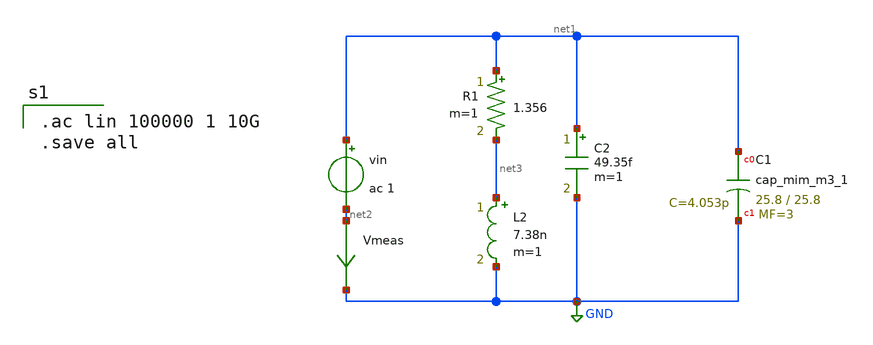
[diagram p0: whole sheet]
** sch_path: XSCHEM/ANTENNA/RLC_CSTXschem.sch
**.subckt RLC_CSTXschem
vin net1 net2 ac 1
XC1 net1 GND sky130_fd_pr__cap_mim_m3_1 W=25.8 L=25.8 MF=3 m=3
Vmeas net2 GND 0
.save i(vmeas)
R1 net1 net3 1.356 m=1
L2 net3 GND 7.38n m=1
C2 net1 GND 49.35f m=1
**** begin user architecture code

.ac lin 100000 1 10G
.save all


** opencircuitdesign pdks install
.lib $::SKYWATER_MODELS/sky130.lib.spice ff
.include /usr/local/share/pdk/sky130A/libs.ref/sky130_fd_sc_hd/spice/sky130_fd_sc_hd.spice

**** end user architecture code
**.ends
.GLOBAL GND
.end
